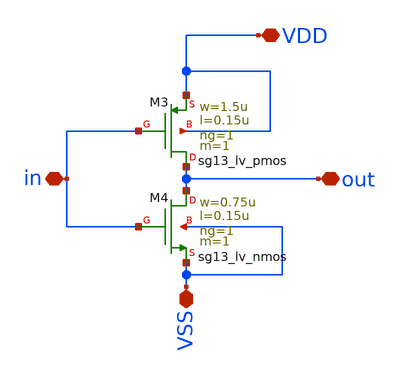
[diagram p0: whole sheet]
** sch_path: design/blocks/inverter/schematic/inverter.sch
**.subckt inverter VDD in out VSS
*.iopin VDD
*.iopin in
*.iopin out
*.iopin VSS
XM3 out in VDD VDD sg13_lv_pmos w=1.5u l=0.15u ng=1 m=1 mm_ok=1
XM4 out in VSS VSS sg13_lv_nmos w=0.75u l=0.15u ng=1 m=1 mm_ok=1
**.ends
.end
